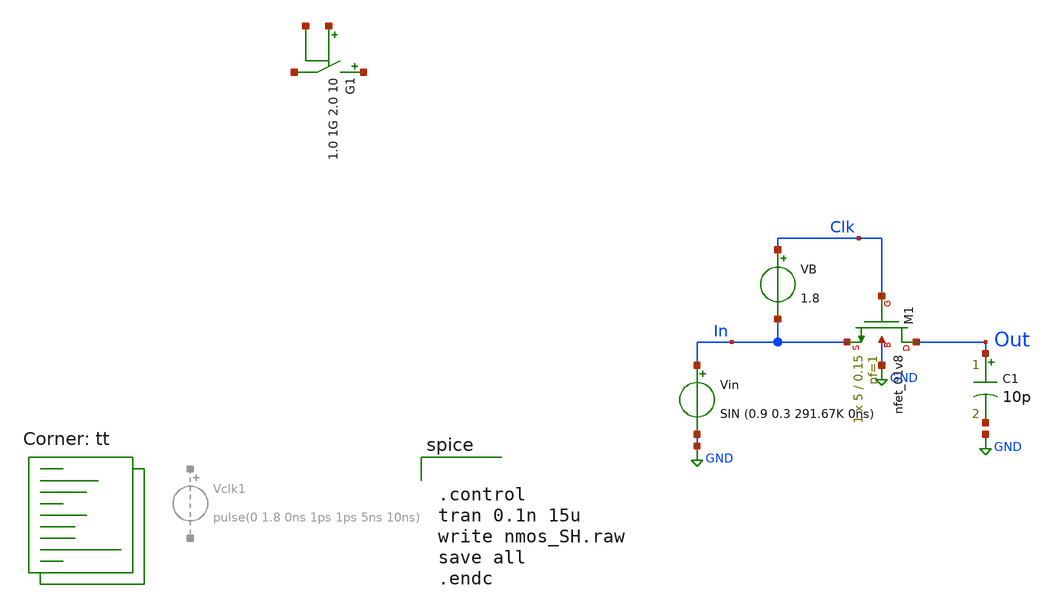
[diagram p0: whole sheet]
** sch_path: SampleHold/ideal_SH.sch
**.subckt ideal_SH
XM1 Out Clk In GND sky130_fd_pr__nfet_01v8 L=0.15 W=5 nf=1 ad='int((nf+1)/2) * W/nf * 0.29' as='int((nf+2)/2) * W/nf * 0.29'
+ pd='2*int((nf+1)/2) * (W/nf + 0.29)' ps='2*int((nf+2)/2) * (W/nf + 0.29)' nrd='0.29 / W' nrs='0.29 / W'
+ sa=0 sb=0 sd=0 mult=1 m=1
C1 Out net1 10p m=1
VB Clk In 1.8
Vin In GND SIN (0.9 0.3 291.67K 0ns)
G1 net3 net4 vcr pwl(1) net2 net5 1.0 1G 2.0 10
**** begin user architecture code
.lib $::SKYWATER_MODELS/sky130.lib.spice tt


.control
tran 0.1n 15u
write nmos_SH.raw
save all
.endc


**** end user architecture code
**.ends
.GLOBAL GND
.end
